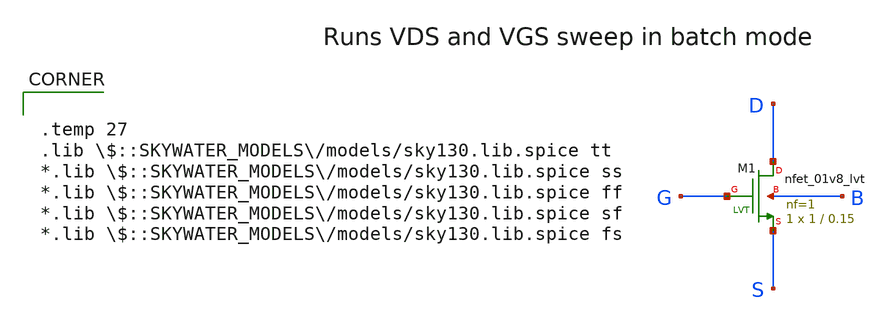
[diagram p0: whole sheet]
** sch_path: nmos_tb.sch
**.subckt nmos_tb
XM1 D G S B sky130_fd_pr__nfet_01v8_lvt L=0.15 W=1 nf=1 ad='int((nf+1)/2) * W/nf * 0.29' as='int((nf+2)/2) * W/nf * 0.29'
+ pd='2*int((nf+1)/2) * (W/nf + 0.29)' ps='2*int((nf+2)/2) * (W/nf + 0.29)' nrd='0.29 / W' nrs='0.29 / W'
+ sa=0 sb=0 sd=0 mult=1 m=1
**** begin user architecture code


Vg G 0 1.8
Vs S 0 0
Vd D 0 1.8
Vb B 0 0

*.dc Vd 0 1.8 0.1 Vg 0 1.8 0.6
.dc Vd 0 1.8 0.1
.save v(G) v(D) v(S) v(B)
.save @m.xm1.msky130_fd_pr__nfet_01v8_lvt[gm]
.save @m.xm1.msky130_fd_pr__nfet_01v8_lvt[gmbs]
.save @m.xm1.msky130_fd_pr__nfet_01v8_lvt[gds]
.save @m.xm1.msky130_fd_pr__nfet_01v8_lvt[vdsat]
.save @m.xm1.msky130_fd_pr__nfet_01v8_lvt[vth]
.save @m.xm1.msky130_fd_pr__nfet_01v8_lvt[id]
.save @m.xm1.msky130_fd_pr__nfet_01v8_lvt[vbs]
.save @m.xm1.msky130_fd_pr__nfet_01v8_lvt[vgs]
.save @m.xm1.msky130_fd_pr__nfet_01v8_lvt[vds]
.save @m.xm1.msky130_fd_pr__nfet_01v8_lvt[cgg]
.save @m.xm1.msky130_fd_pr__nfet_01v8_lvt[cgs]
.save @m.xm1.msky130_fd_pr__nfet_01v8_lvt[cgd]
.save @m.xm1.msky130_fd_pr__nfet_01v8_lvt[cbg]
.save @m.xm1.msky130_fd_pr__nfet_01v8_lvt[cbd]
.save @m.xm1.msky130_fd_pr__nfet_01v8_lvt[cbs]
.save @m.xm1.msky130_fd_pr__nfet_01v8_lvt[cdg]
.save @m.xm1.msky130_fd_pr__nfet_01v8_lvt[cdd]
.save @m.xm1.msky130_fd_pr__nfet_01v8_lvt[cds]
.save @m.xm1.msky130_fd_pr__nfet_01v8_lvt[csg]
.save @m.xm1.msky130_fd_pr__nfet_01v8_lvt[csd]
.save @m.xm1.msky130_fd_pr__nfet_01v8_lvt[css]
.save @m.xm1.msky130_fd_pr__nfet_01v8_lvt[cgb]
.save @m.xm1.msky130_fd_pr__nfet_01v8_lvt[cdb]
.save @m.xm1.msky130_fd_pr__nfet_01v8_lvt[csb]
.save @m.xm1.msky130_fd_pr__nfet_01v8_lvt[cbb]
.save @m.xm1.msky130_fd_pr__nfet_01v8_lvt[capbd]
.save @m.xm1.msky130_fd_pr__nfet_01v8_lvt[capbs]


*.control
*save all
*dc Vd 0 1.8 0.05 Vg 0 1.8 0.3
*plot all.vd1#branch vs D1v8
*plot all.vd2#branch vs D1v8
*plot all.vd3#branch vs D3v3
*plot all.vd4#branch vs D5v0
*plot all.vd5#branch vs D10v5
*plot all.vd6#branch vs D16v0
*plot all.vd8#branch vs D1v8
*plot all.vd7#branch vs D1v8
*save @m.xm1.msky130_fd_pr__nfet_01v8_lvt[gm]
*op
*write test_nmos.raw
*.endc



.temp 27
.lib $::SKYWATER_MODELS/models/sky130.lib.spice tt
*.lib $::SKYWATER_MODELS/models/sky130.lib.spice ss
*.lib $::SKYWATER_MODELS/models/sky130.lib.spice ff
*.lib $::SKYWATER_MODELS/models/sky130.lib.spice sf
*.lib $::SKYWATER_MODELS/models/sky130.lib.spice fs

**** end user architecture code
**.ends
.end
